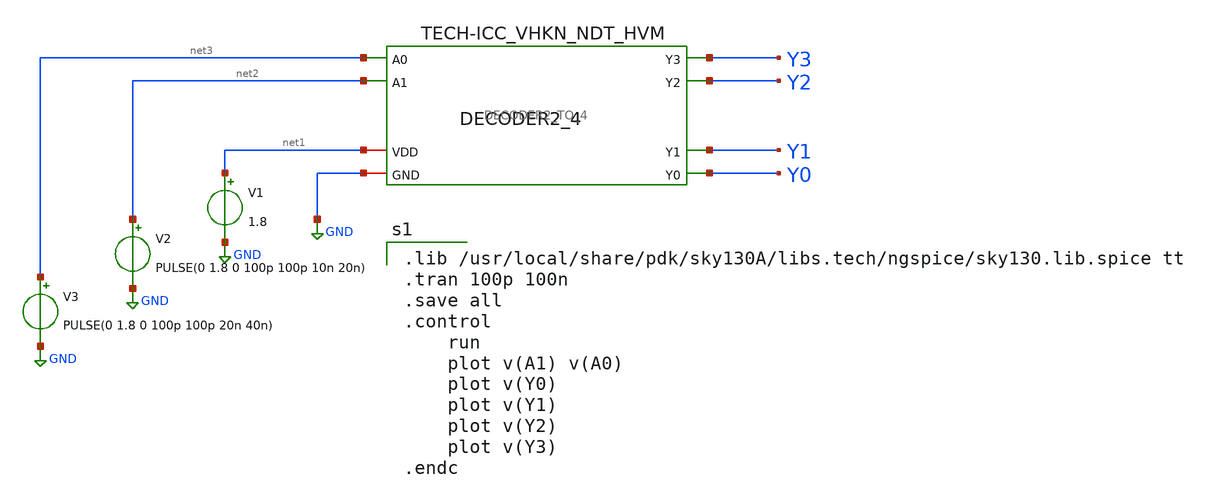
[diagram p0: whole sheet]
** sch_path: DECODER3TO8/Schematic/CMOS_DECODER2_4.sch
**.subckt CMOS_DECODER2_4
x1 net1 net3 GND net2 Y3 Y2 Y1 Y0 DECODER2_TO_4
V1 net1 GND 1.8
V2 net2 GND PULSE(0 1.8 0 100p 100p 10n 20n)
V3 net3 GND PULSE(0 1.8 0 100p 100p 20n 40n)
**** begin user architecture code

.lib /usr/local/share/pdk/sky130A/libs.tech/ngspice/sky130.lib.spice tt
.tran 100p 100n
.save all
.control
    run
    plot v(A1) v(A0)
    plot v(Y0)
    plot v(Y1)
    plot v(Y2)
    plot v(Y3)
.endc


**** end user architecture code
**.ends
.GLOBAL GND
.end
